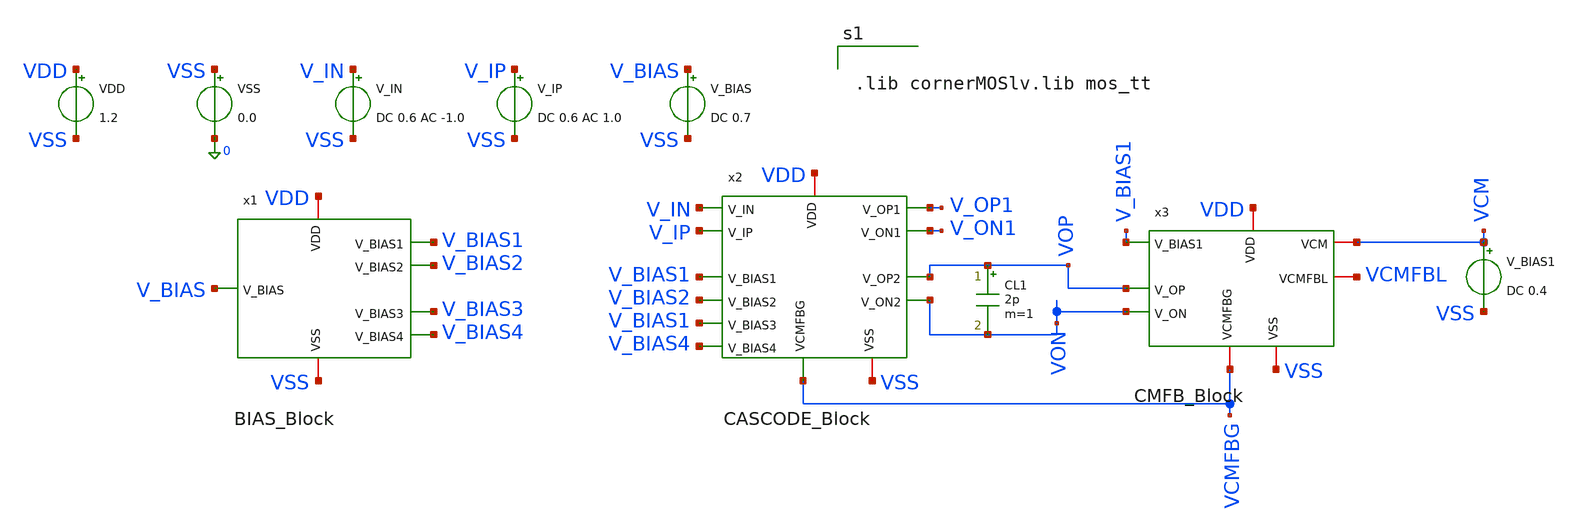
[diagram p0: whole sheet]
** sch_path: two-stage-ota-with-cmfb/Simulation/TEST_DC_OP.sch
**.subckt TEST_DC_OP
VDD VDD VSS 1.2
VSS VSS 0 0.0
V_IN V_IN VSS DC 0.6 AC -1.0
V_IP V_IP VSS DC 0.6 AC 1.0
V_BIAS V_BIAS VSS DC 0.7
V_BIAS1 VCM VSS DC 0.4
CL1 VOP VON 2p m=1
x1 VSS V_BIAS4 V_BIAS2 V_BIAS3 VDD V_BIAS1 V_BIAS BIAS_Block
x2 VDD V_BIAS1 V_IN V_IP V_BIAS2 V_ON1 V_OP1 V_BIAS1 VON VOP VCMFBG V_BIAS4 VSS CASCODE_Block
x3 VDD V_BIAS1 VCM VOP VON VCMFBL VCMFBG VSS CMFB_Block
**** begin user architecture code


.lib cornerMOSlv.lib mos_tt




.control
op

echo '=========================================================================='
echo '          A1. CHECK SATURATION & DC PARAMETERS'
echo '=========================================================================='

echo '--- 1. MAIN CASCODE & CS STAGE (x2) ---'
echo '--------------------------------------------------------------------------'
print @n.x2.xm0.nsg13_lv_pmos[vds]     @n.x2.xm0.nsg13_lv_pmos[vgs]     @n.x2.xm0.nsg13_lv_pmos[vth]
+     @n.x2.xm0.nsg13_lv_pmos[ids]
echo '--------------------------------------------------------------------------'
print @n.x2.xm1.nsg13_lv_pmos[vds]     @n.x2.xm1.nsg13_lv_pmos[vgs]     @n.x2.xm1.nsg13_lv_pmos[vth]
+     @n.x2.xm1.nsg13_lv_pmos[ids]
echo '--------------------------------------------------------------------------'
print @n.x2.xm2.nsg13_lv_pmos[vds]     @n.x2.xm2.nsg13_lv_pmos[vgs]     @n.x2.xm2.nsg13_lv_pmos[vth]
+     @n.x2.xm2.nsg13_lv_pmos[ids]
echo '--------------------------------------------------------------------------'
print @n.x2.xm3.nsg13_lv_pmos[vds]     @n.x2.xm3.nsg13_lv_pmos[vgs]     @n.x2.xm3.nsg13_lv_pmos[vth]
+     @n.x2.xm3.nsg13_lv_pmos[ids]
echo '--------------------------------------------------------------------------'
print @n.x2.xm4.nsg13_lv_pmos[vds]     @n.x2.xm4.nsg13_lv_pmos[vgs]     @n.x2.xm4.nsg13_lv_pmos[vth]
+     @n.x2.xm4.nsg13_lv_pmos[ids]
echo '--------------------------------------------------------------------------'
print @n.x2.xm5.nsg13_lv_nmos[vds]     @n.x2.xm5.nsg13_lv_nmos[vgs]     @n.x2.xm5.nsg13_lv_nmos[vth]
+     @n.x2.xm5.nsg13_lv_nmos[ids]
echo '--------------------------------------------------------------------------'
print @n.x2.xm6.nsg13_lv_nmos[vds]     @n.x2.xm6.nsg13_lv_nmos[vgs]     @n.x2.xm6.nsg13_lv_nmos[vth]
+     @n.x2.xm6.nsg13_lv_nmos[ids]
echo '--------------------------------------------------------------------------'
print @n.x2.xm7.nsg13_lv_nmos[vds]     @n.x2.xm7.nsg13_lv_nmos[vgs]     @n.x2.xm7.nsg13_lv_nmos[vth]
+     @n.x2.xm7.nsg13_lv_nmos[ids]
echo '--------------------------------------------------------------------------'
print @n.x2.xm8.nsg13_lv_nmos[vds]     @n.x2.xm8.nsg13_lv_nmos[vgs]     @n.x2.xm8.nsg13_lv_nmos[vth]
+     @n.x2.xm8.nsg13_lv_nmos[ids]
echo '--------------------------------------------------------------------------'
print @n.x2.xm_cs1.nsg13_lv_pmos[vds]  @n.x2.xm_cs1.nsg13_lv_pmos[vgs]
+  @n.x2.xm_cs1.nsg13_lv_pmos[vth]  @n.x2.xm_cs1.nsg13_lv_pmos[ids]
echo '--------------------------------------------------------------------------'
print @n.x2.xm_cs2.nsg13_lv_pmos[vds]  @n.x2.xm_cs2.nsg13_lv_pmos[vgs]
+  @n.x2.xm_cs2.nsg13_lv_pmos[vth]  @n.x2.xm_cs2.nsg13_lv_pmos[ids]
echo '--------------------------------------------------------------------------'
print @n.x2.xm_l1.nsg13_lv_nmos[vds]   @n.x2.xm_l1.nsg13_lv_nmos[vgs]
+   @n.x2.xm_l1.nsg13_lv_nmos[vth]   @n.x2.xm_l1.nsg13_lv_nmos[ids]
echo '--------------------------------------------------------------------------'
print @n.x2.xm_l2.nsg13_lv_nmos[vds]   @n.x2.xm_l2.nsg13_lv_nmos[vgs]
+   @n.x2.xm_l2.nsg13_lv_nmos[vth]   @n.x2.xm_l2.nsg13_lv_nmos[ids]

echo '=========================================================================='
echo '--- 2. CMFB BLOCK (x3) ---'
echo '--------------------------------------------------------------------------'
print @n.x3.xm14.nsg13_lv_pmos[vds]    @n.x3.xm14.nsg13_lv_pmos[vgs]
+    @n.x3.xm14.nsg13_lv_pmos[vth]    @n.x3.xm14.nsg13_lv_pmos[ids]
echo '--------------------------------------------------------------------------'
print @n.x3.xm16.nsg13_lv_pmos[vds]    @n.x3.xm16.nsg13_lv_pmos[vgs]
+    @n.x3.xm16.nsg13_lv_pmos[vth]    @n.x3.xm16.nsg13_lv_pmos[ids]
echo '--------------------------------------------------------------------------'
print @n.x3.xm20.nsg13_lv_nmos[vds]    @n.x3.xm20.nsg13_lv_nmos[vgs]
+    @n.x3.xm20.nsg13_lv_nmos[vth]    @n.x3.xm20.nsg13_lv_nmos[ids]

echo '=========================================================================='
echo '--- 3. BIAS BLOCK (x1) ---'
echo '--------------------------------------------------------------------------'
print @n.x1.xm2.nsg13_lv_pmos[vds]     @n.x1.xm2.nsg13_lv_pmos[vgs]     @n.x1.xm2.nsg13_lv_pmos[vth]
+     @n.x1.xm2.nsg13_lv_pmos[ids]
echo '--------------------------------------------------------------------------'
print @n.x1.xm1.nsg13_lv_nmos[vds]     @n.x1.xm1.nsg13_lv_nmos[vgs]     @n.x1.xm1.nsg13_lv_nmos[vth]
+     @n.x1.xm1.nsg13_lv_nmos[ids]
echo '--------------------------------------------------------------------------'
print @n.x1.xm10.nsg13_lv_nmos[vds]    @n.x1.xm10.nsg13_lv_nmos[vgs]
+    @n.x1.xm10.nsg13_lv_nmos[vth]    @n.x1.xm10.nsg13_lv_nmos[ids]
echo '--------------------------------------------------------------------------'
print @n.x1.xm11.nsg13_lv_nmos[vds]    @n.x1.xm11.nsg13_lv_nmos[vgs]
+    @n.x1.xm11.nsg13_lv_nmos[vth]    @n.x1.xm11.nsg13_lv_nmos[ids]

echo '=========================================================================='
echo '          A2. VERIFY OUTPUT COMMON-MODE VOLTAGE (TARGET: 0.6V)'
echo '=========================================================================='
let v_cm_out = (v(vop) + v(von)) / 2
let v_diff_offset = v(vop) - v(von)
print v(vop) v(von) v_cm_out v_diff_offset

echo '=========================================================================='
echo '          A3. REPORT QUIESCENT CURRENT AND POWER CONSUMPTION'
echo '=========================================================================='
* Dong qua tung khoi tinh tu ids cua cac transistor nguon cap (Top PMOS):
let i_cascode = abs(@n.x2.xm0.nsg13_lv_pmos[ids])
let i_cs      = abs(@n.x2.xm_cs1.nsg13_lv_pmos[ids]) + abs(@n.x2.xm_cs2.nsg13_lv_pmos[ids])
let i_cmfb    = abs(@n.x3.xm14.nsg13_lv_pmos[ids]) + abs(@n.x3.xm15.nsg13_lv_pmos[ids])
let i_bias    = abs(@n.x1.xm2.nsg13_lv_pmos[ids]) + abs(@n.x1.xm4.nsg13_lv_pmos[ids]) +
+ abs(@n.x1.xm8.nsg13_lv_pmos[ids])

let p_cascode = i_cascode * 1.2
let p_cs      = i_cs * 1.2
let p_cmfb    = i_cmfb * 1.2
let p_bias    = i_bias * 1.2

let i_total   = i_cascode + i_cs + i_cmfb + i_bias
let p_total   = i_total * 1.2

print i_cascode p_cascode
print i_cs p_cs
print i_cmfb p_cmfb
print i_bias p_bias
print i_total p_total

.endc


**** end user architecture code
**.ends
.end
